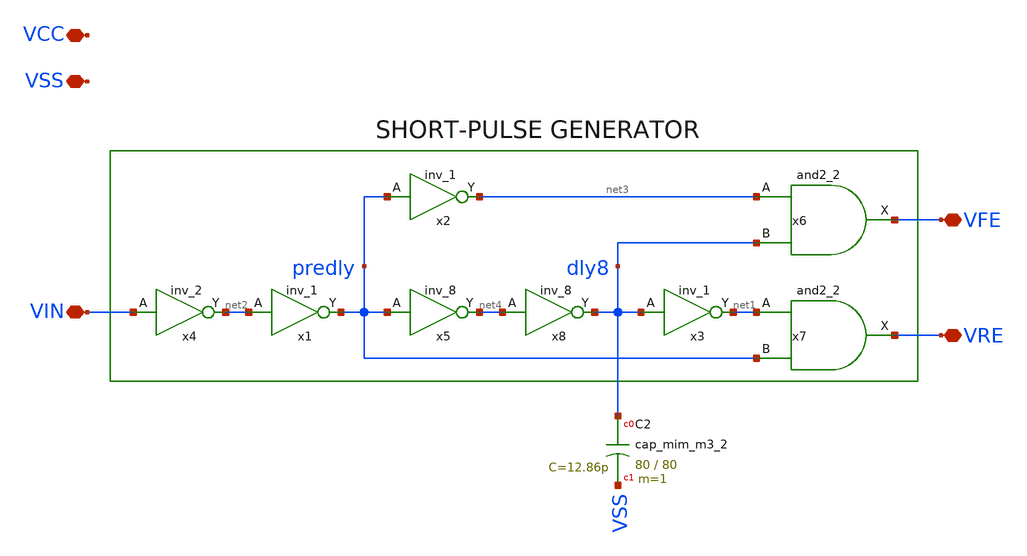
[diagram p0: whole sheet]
** sch_path: xschem/pulse_generator.sch
**.subckt pulse_generator VIN VFE VRE VCC VSS
*.iopin VIN
*.iopin VFE
*.iopin VRE
*.iopin VCC
*.iopin VSS
x1 net2 VSS VSS VCC VCC predly sky130_fd_sc_hd__inv_1
x2 predly VSS VSS VCC VCC net3 sky130_fd_sc_hd__inv_1
x3 dly8 VSS VSS VCC VCC net1 sky130_fd_sc_hd__inv_1
x4 VIN VSS VSS VCC VCC net2 sky130_fd_sc_hd__inv_2
x5 predly VSS VSS VCC VCC net4 sky130_fd_sc_hd__inv_8
x6 net3 dly8 VSS VSS VCC VCC VFE sky130_fd_sc_hd__and2_2
x7 net1 predly VSS VSS VCC VCC VRE sky130_fd_sc_hd__and2_2
XC2 dly8 VSS sky130_fd_pr__cap_mim_m3_2 W=80 L=80 MF=1 m=1
x8 net4 VSS VSS VCC VCC dly8 sky130_fd_sc_hd__inv_8
**.ends
.end
